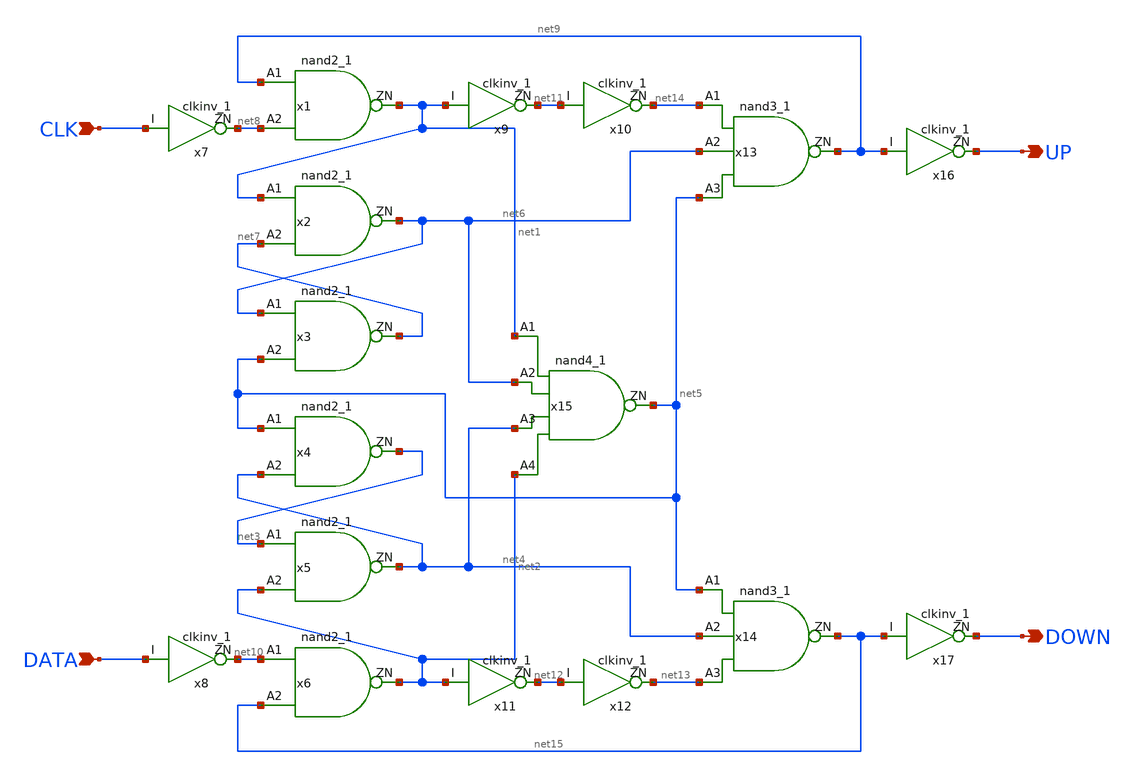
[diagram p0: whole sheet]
** sch_path: pfd2.sch
**.subckt pfd2 DATA CLK UP DOWN
*.ipin DATA
*.ipin CLK
*.opin UP
*.opin DOWN
x1 net9 net8 net1 VDD VDD GND GND gf180mcu_fd_sc_mcu7t5v0__nand2_1
x7 CLK net8 VDD VDD GND GND gf180mcu_fd_sc_mcu7t5v0__clkinv_1
x13 net14 net6 net5 net9 VDD VDD GND GND gf180mcu_fd_sc_mcu7t5v0__nand3_1
x14 net5 net4 net13 net15 VDD VDD GND GND gf180mcu_fd_sc_mcu7t5v0__nand3_1
x15 net1 net6 net4 net2 net5 VDD VDD GND GND gf180mcu_fd_sc_mcu7t5v0__nand4_1
x2 net1 net7 net6 VDD VDD GND GND gf180mcu_fd_sc_mcu7t5v0__nand2_1
x3 net6 net5 net7 VDD VDD GND GND gf180mcu_fd_sc_mcu7t5v0__nand2_1
x4 net5 net4 net3 VDD VDD GND GND gf180mcu_fd_sc_mcu7t5v0__nand2_1
x5 net3 net2 net4 VDD VDD GND GND gf180mcu_fd_sc_mcu7t5v0__nand2_1
x6 net10 net15 net2 VDD VDD GND GND gf180mcu_fd_sc_mcu7t5v0__nand2_1
x8 DATA net10 VDD VDD GND GND gf180mcu_fd_sc_mcu7t5v0__clkinv_1
x9 net1 net11 VDD VDD GND GND gf180mcu_fd_sc_mcu7t5v0__clkinv_1
x10 net11 net14 VDD VDD GND GND gf180mcu_fd_sc_mcu7t5v0__clkinv_1
x11 net2 net12 VDD VDD GND GND gf180mcu_fd_sc_mcu7t5v0__clkinv_1
x12 net12 net13 VDD VDD GND GND gf180mcu_fd_sc_mcu7t5v0__clkinv_1
x16 net9 UP VDD VDD GND GND gf180mcu_fd_sc_mcu7t5v0__clkinv_1
x17 net15 DOWN VDD VDD GND GND gf180mcu_fd_sc_mcu7t5v0__clkinv_1
**.ends
.end
